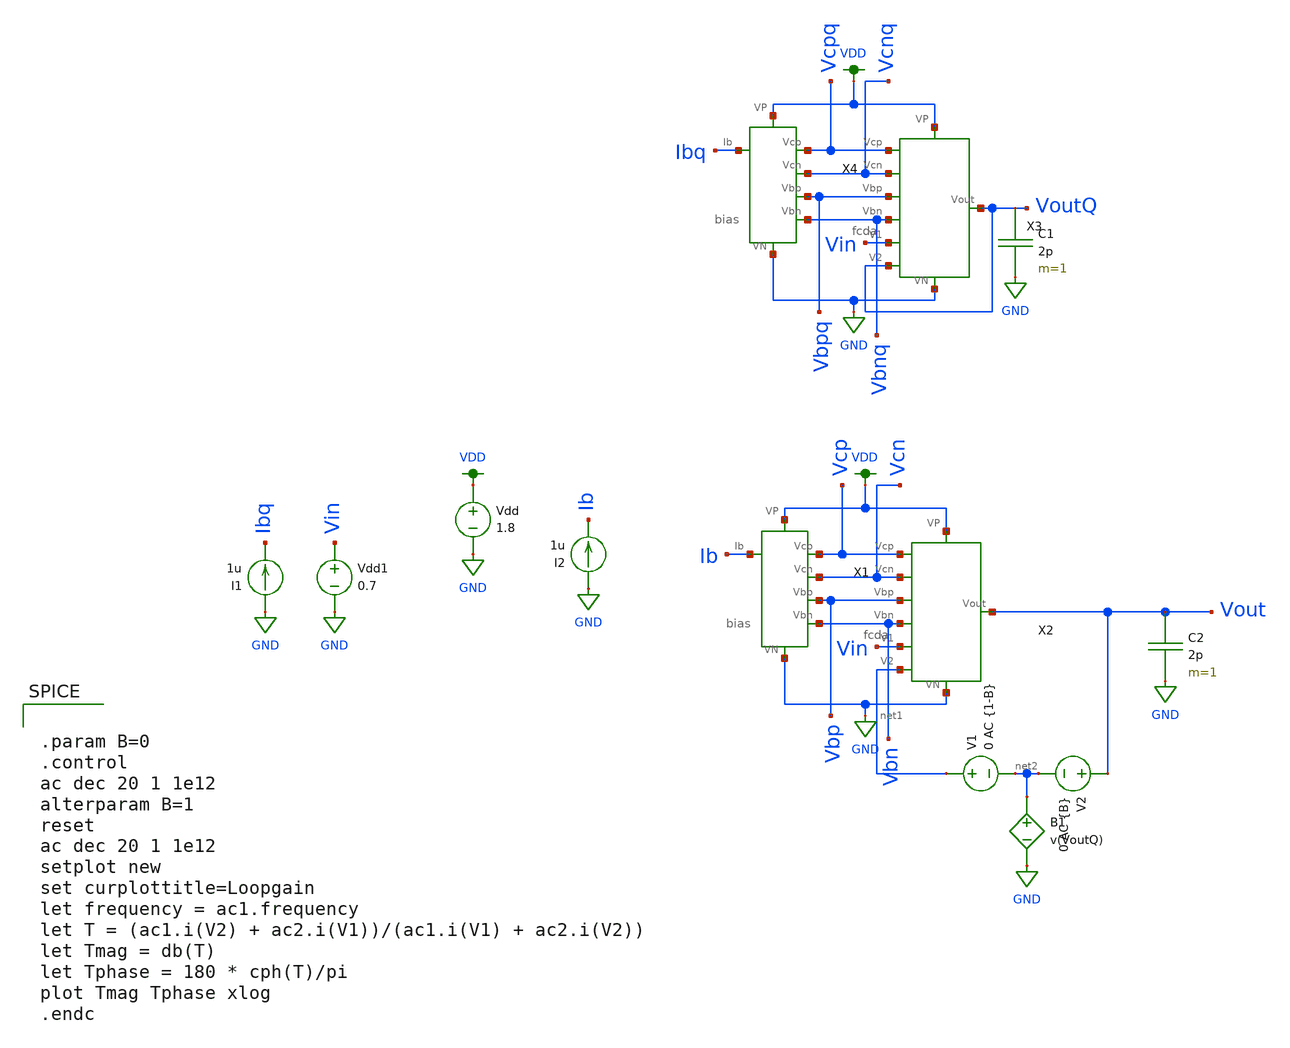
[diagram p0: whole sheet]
** sch_path: mp3/schematic/amp_tran_loop_gain.sch
**.subckt amp_tran_loop_gain
Vdd1 Vin GND 0.7
I1 GND Ibq 1u
Vdd VDD GND 1.8
C2 Vout GND 2p m=1
X2 Vcp Vcn Vbp Vbn Vin net1 VDD GND Vout fcda
X1 VDD GND Ib Vcp Vcn Vbp Vbn bias
C1 VoutQ GND 2p m=1
X3 Vcpq Vcnq Vbpq Vbnq Vin VoutQ VDD GND VoutQ fcda
X4 VDD GND Ibq Vcpq Vcnq Vbpq Vbnq bias
V2 Vout net2 0 AC {B}
V1 net1 net2 0 AC {1-B}
B1 net2 GND V=v(VoutQ)
I2 GND Ib 1u
**** begin user architecture code

.option wnflag=1
.lib ~/skywater/skywater-pdk/libraries/sky130_fd_pr_ngspice/latest/models/sky130.lib.spice tt



.param B=0
.control
ac dec 20 1 1e12
alterparam B=1
reset
ac dec 20 1 1e12
setplot new
set curplottitle=Loopgain
let frequency = ac1.frequency
let T = (ac1.i(V2) + ac2.i(V1))/(ac1.i(V1) + ac2.i(V2))
let Tmag = db(T)
let Tphase = 180 * cph(T)/pi
plot Tmag Tphase xlog
.endc


**** end user architecture code
**.ends

* expanding   symbol:  /home/madvlsi/madvlsi/mp3/schematic/fcda.sym # of pins=9
** sym_path: mp3/schematic/fcda.sym
** sch_path: mp3/schematic/fcda.sch
.subckt fcda Vcp Vcn Vbp Vbn V1 V2 VP VN Vout
*.iopin VP
*.iopin VN
*.ipin Vbp
*.ipin V2
*.ipin V1
*.ipin Vbn
*.ipin Vcp
*.ipin Vcn
*.opin Vout
XM1 net2 Vbp VP VDD sky130_fd_pr__pfet_01v8 L=0.5 W=12 nf=1 ad='int((nf+1)/2) * W/nf * 0.29' as='int((nf+2)/2) * W/nf * 0.29'
+ pd='2*int((nf+1)/2) * (W/nf + 0.29)' ps='2*int((nf+2)/2) * (W/nf + 0.29)' nrd='0.29 / W' nrs='0.29 / W'
+ sa=0 sb=0 sd=0 mult=1 m=1
XM2 net2 V1 net1 GND sky130_fd_pr__nfet_01v8 L=0.5 W=12 nf=1 ad='int((nf+1)/2) * W/nf * 0.29' as='int((nf+2)/2) * W/nf * 0.29'
+ pd='2*int((nf+1)/2) * (W/nf + 0.29)' ps='2*int((nf+2)/2) * (W/nf + 0.29)' nrd='0.29 / W' nrs='0.29 / W'
+ sa=0 sb=0 sd=0 mult=1 m=1
XM3 net3 V2 net1 GND sky130_fd_pr__nfet_01v8 L=0.5 W=12 nf=1 ad='int((nf+1)/2) * W/nf * 0.29' as='int((nf+2)/2) * W/nf * 0.29'
+ pd='2*int((nf+1)/2) * (W/nf + 0.29)' ps='2*int((nf+2)/2) * (W/nf + 0.29)' nrd='0.29 / W' nrs='0.29 / W'
+ sa=0 sb=0 sd=0 mult=1 m=1
XM4 net1 Vbn VN GND sky130_fd_pr__nfet_01v8 L=0.5 W=12 nf=1 ad='int((nf+1)/2) * W/nf * 0.29' as='int((nf+2)/2) * W/nf * 0.29'
+ pd='2*int((nf+1)/2) * (W/nf + 0.29)' ps='2*int((nf+2)/2) * (W/nf + 0.29)' nrd='0.29 / W' nrs='0.29 / W'
+ sa=0 sb=0 sd=0 mult=1 m=1
XM5 net3 Vbp VP VDD sky130_fd_pr__pfet_01v8 L=0.5 W=12 nf=1 ad='int((nf+1)/2) * W/nf * 0.29' as='int((nf+2)/2) * W/nf * 0.29'
+ pd='2*int((nf+1)/2) * (W/nf + 0.29)' ps='2*int((nf+2)/2) * (W/nf + 0.29)' nrd='0.29 / W' nrs='0.29 / W'
+ sa=0 sb=0 sd=0 mult=1 m=1
XM6 Vout Vcp net3 VDD sky130_fd_pr__pfet_01v8 L=0.5 W=12 nf=1 ad='int((nf+1)/2) * W/nf * 0.29' as='int((nf+2)/2) * W/nf * 0.29'
+ pd='2*int((nf+1)/2) * (W/nf + 0.29)' ps='2*int((nf+2)/2) * (W/nf + 0.29)' nrd='0.29 / W' nrs='0.29 / W'
+ sa=0 sb=0 sd=0 mult=1 m=1
XM7 net4 Vcp net2 VDD sky130_fd_pr__pfet_01v8 L=0.5 W=12 nf=1 ad='int((nf+1)/2) * W/nf * 0.29' as='int((nf+2)/2) * W/nf * 0.29'
+ pd='2*int((nf+1)/2) * (W/nf + 0.29)' ps='2*int((nf+2)/2) * (W/nf + 0.29)' nrd='0.29 / W' nrs='0.29 / W'
+ sa=0 sb=0 sd=0 mult=1 m=1
XM8 net4 Vcn net5 GND sky130_fd_pr__nfet_01v8 L=0.5 W=12 nf=1 ad='int((nf+1)/2) * W/nf * 0.29' as='int((nf+2)/2) * W/nf * 0.29'
+ pd='2*int((nf+1)/2) * (W/nf + 0.29)' ps='2*int((nf+2)/2) * (W/nf + 0.29)' nrd='0.29 / W' nrs='0.29 / W'
+ sa=0 sb=0 sd=0 mult=1 m=1
XM9 net6 net4 VN GND sky130_fd_pr__nfet_01v8 L=0.5 W=12 nf=1 ad='int((nf+1)/2) * W/nf * 0.29' as='int((nf+2)/2) * W/nf * 0.29'
+ pd='2*int((nf+1)/2) * (W/nf + 0.29)' ps='2*int((nf+2)/2) * (W/nf + 0.29)' nrd='0.29 / W' nrs='0.29 / W'
+ sa=0 sb=0 sd=0 mult=1 m=1
XM10 Vout Vcn net6 GND sky130_fd_pr__nfet_01v8 L=0.5 W=12 nf=1 ad='int((nf+1)/2) * W/nf * 0.29' as='int((nf+2)/2) * W/nf * 0.29'
+ pd='2*int((nf+1)/2) * (W/nf + 0.29)' ps='2*int((nf+2)/2) * (W/nf + 0.29)' nrd='0.29 / W' nrs='0.29 / W'
+ sa=0 sb=0 sd=0 mult=1 m=1
XM11 VN net4 net5 GND sky130_fd_pr__nfet_01v8 L=0.5 W=12 nf=1 ad='int((nf+1)/2) * W/nf * 0.29' as='int((nf+2)/2) * W/nf * 0.29'
+ pd='2*int((nf+1)/2) * (W/nf + 0.29)' ps='2*int((nf+2)/2) * (W/nf + 0.29)' nrd='0.29 / W' nrs='0.29 / W'
+ sa=0 sb=0 sd=0 mult=1 m=1
.ends


* expanding   symbol:  /home/madvlsi/madvlsi/mp3/schematic/bias.sym # of pins=7
** sym_path: mp3/schematic/bias.sym
** sch_path: mp3/schematic/bias.sch
.subckt bias VP VN Ib Vcp Vcn Vbp Vbn
*.iopin VP
*.iopin VN
*.opin Vcp
*.opin Vcn
*.opin Vbp
*.iopin Ib
*.opin Vbn
XM1 net3 net1 VP VDD sky130_fd_pr__pfet_01v8 L=0.5 W=12 nf=1 ad='int((nf+1)/2) * W/nf * 0.29' as='int((nf+2)/2) * W/nf * 0.29'
+ pd='2*int((nf+1)/2) * (W/nf + 0.29)' ps='2*int((nf+2)/2) * (W/nf + 0.29)' nrd='0.29 / W' nrs='0.29 / W'
+ sa=0 sb=0 sd=0 mult=1 m=1
XM2 net1 net1 net3 VDD sky130_fd_pr__pfet_01v8 L=0.5 W=12 nf=1 ad='int((nf+1)/2) * W/nf * 0.29' as='int((nf+2)/2) * W/nf * 0.29'
+ pd='2*int((nf+1)/2) * (W/nf + 0.29)' ps='2*int((nf+2)/2) * (W/nf + 0.29)' nrd='0.29 / W' nrs='0.29 / W'
+ sa=0 sb=0 sd=0 mult=4 m=4
XM3 net3 Vcp Vcp VDD sky130_fd_pr__pfet_01v8 L=0.5 W=12 nf=1 ad='int((nf+1)/2) * W/nf * 0.29' as='int((nf+2)/2) * W/nf * 0.29'
+ pd='2*int((nf+1)/2) * (W/nf + 0.29)' ps='2*int((nf+2)/2) * (W/nf + 0.29)' nrd='0.29 / W' nrs='0.29 / W'
+ sa=0 sb=0 sd=0 mult=1 m=1
XM4 net1 Ib VN GND sky130_fd_pr__nfet_01v8 L=0.5 W=12 nf=1 ad='int((nf+1)/2) * W/nf * 0.29' as='int((nf+2)/2) * W/nf * 0.29'
+ pd='2*int((nf+1)/2) * (W/nf + 0.29)' ps='2*int((nf+2)/2) * (W/nf + 0.29)' nrd='0.29 / W' nrs='0.29 / W'
+ sa=0 sb=0 sd=0 mult=1/6 m=1/6
XM5 Vcp Ib VN GND sky130_fd_pr__nfet_01v8 L=0.5 W=12 nf=1 ad='int((nf+1)/2) * W/nf * 0.29' as='int((nf+2)/2) * W/nf * 0.29'
+ pd='2*int((nf+1)/2) * (W/nf + 0.29)' ps='2*int((nf+2)/2) * (W/nf + 0.29)' nrd='0.29 / W' nrs='0.29 / W'
+ sa=0 sb=0 sd=0 mult=1 m=1
XM6 net4 Ib VN GND sky130_fd_pr__nfet_01v8 L=0.5 W=12 nf=1 ad='int((nf+1)/2) * W/nf * 0.29' as='int((nf+2)/2) * W/nf * 0.29'
+ pd='2*int((nf+1)/2) * (W/nf + 0.29)' ps='2*int((nf+2)/2) * (W/nf + 0.29)' nrd='0.29 / W' nrs='0.29 / W'
+ sa=0 sb=0 sd=0 mult=1 m=1
XM7 Vbn Vbp VP VDD sky130_fd_pr__pfet_01v8 L=0.5 W=12 nf=1 ad='int((nf+1)/2) * W/nf * 0.29' as='int((nf+2)/2) * W/nf * 0.29'
+ pd='2*int((nf+1)/2) * (W/nf + 0.29)' ps='2*int((nf+2)/2) * (W/nf + 0.29)' nrd='0.29 / W' nrs='0.29 / W'
+ sa=0 sb=0 sd=0 mult=1/6 m=1/6
XM8 Vcn Vbp VP VDD sky130_fd_pr__pfet_01v8 L=0.5 W=12 nf=1 ad='int((nf+1)/2) * W/nf * 0.29' as='int((nf+2)/2) * W/nf * 0.29'
+ pd='2*int((nf+1)/2) * (W/nf + 0.29)' ps='2*int((nf+2)/2) * (W/nf + 0.29)' nrd='0.29 / W' nrs='0.29 / W'
+ sa=0 sb=0 sd=0 mult=1 m=1
XM9 net2 Vcn Vcn GND sky130_fd_pr__nfet_01v8 L=0.5 W=12 nf=1 ad='int((nf+1)/2) * W/nf * 0.29' as='int((nf+2)/2) * W/nf * 0.29'
+ pd='2*int((nf+1)/2) * (W/nf + 0.29)' ps='2*int((nf+2)/2) * (W/nf + 0.29)' nrd='0.29 / W' nrs='0.29 / W'
+ sa=0 sb=0 sd=0 mult=1 m=1
XM10 net2 Vbn VN GND sky130_fd_pr__nfet_01v8 L=0.5 W=12 nf=1 ad='int((nf+1)/2) * W/nf * 0.29' as='int((nf+2)/2) * W/nf * 0.29'
+ pd='2*int((nf+1)/2) * (W/nf + 0.29)' ps='2*int((nf+2)/2) * (W/nf + 0.29)' nrd='0.29 / W' nrs='0.29 / W'
+ sa=0 sb=0 sd=0 mult=1 m=1
XM11 Vbn Vbn net2 GND sky130_fd_pr__nfet_01v8 L=0.5 W=12 nf=1 ad='int((nf+1)/2) * W/nf * 0.29' as='int((nf+2)/2) * W/nf * 0.29'
+ pd='2*int((nf+1)/2) * (W/nf + 0.29)' ps='2*int((nf+2)/2) * (W/nf + 0.29)' nrd='0.29 / W' nrs='0.29 / W'
+ sa=0 sb=0 sd=0 mult=4 m=4
XM12 VN Ib Ib GND sky130_fd_pr__nfet_01v8 L=0.5 W=12 nf=1 ad='int((nf+1)/2) * W/nf * 0.29' as='int((nf+2)/2) * W/nf * 0.29'
+ pd='2*int((nf+1)/2) * (W/nf + 0.29)' ps='2*int((nf+2)/2) * (W/nf + 0.29)' nrd='0.29 / W' nrs='0.29 / W'
+ sa=0 sb=0 sd=0 mult=1 m=1
XM13 net4 net4 Vbp VDD sky130_fd_pr__pfet_01v8 L=0.5 W=12 nf=1 ad='int((nf+1)/2) * W/nf * 0.29' as='int((nf+2)/2) * W/nf * 0.29'
+ pd='2*int((nf+1)/2) * (W/nf + 0.29)' ps='2*int((nf+2)/2) * (W/nf + 0.29)' nrd='0.29 / W' nrs='0.29 / W'
+ sa=0 sb=0 sd=0 mult=1 m=1
.ends

.GLOBAL GND
.GLOBAL VDD
.end
